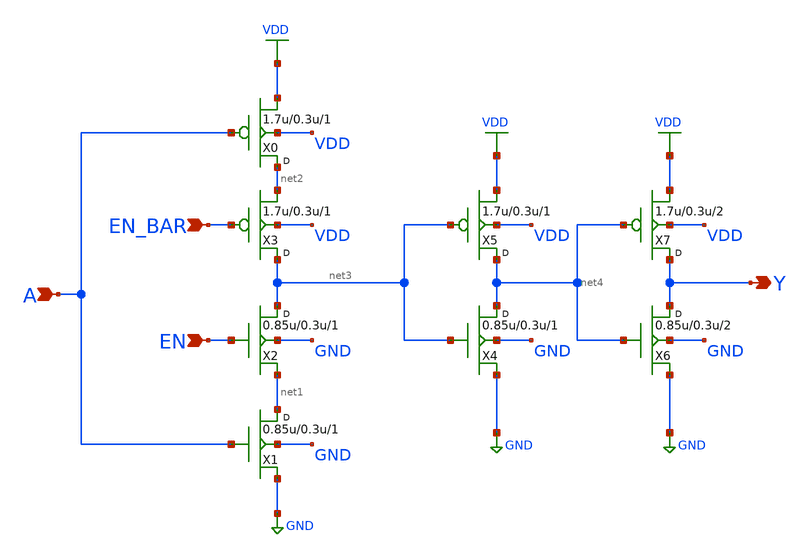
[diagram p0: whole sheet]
** sch_path: lib/12T/tinv2/gf180mcu_osu_sc_tinv_2.sch
**.subckt gf180mcu_osu_sc_tinv_2 A Y EN_BAR EN
*.ipin A
*.opin Y
*.ipin EN_BAR
*.ipin EN
X0 net2 A VDD VDD pmos_3p3 w=1.7u l=0.3u m=1
X1 net1 A GND GND nmos_3p3 w=0.85u l=0.3u m=1
X2 net3 EN net1 GND nmos_3p3 w=0.85u l=0.3u m=1
X3 net3 EN_BAR net2 VDD pmos_3p3 w=1.7u l=0.3u m=1
X4 net4 net3 GND GND nmos_3p3 w=0.85u l=0.3u m=1
X5 net4 net3 VDD VDD pmos_3p3 w=1.7u l=0.3u m=1
X6 Y net4 GND GND nmos_3p3 w=0.85u l=0.3u m=2
X7 Y net4 VDD VDD pmos_3p3 w=1.7u l=0.3u m=2
**.ends
.GLOBAL VDD
.GLOBAL GND
.end
